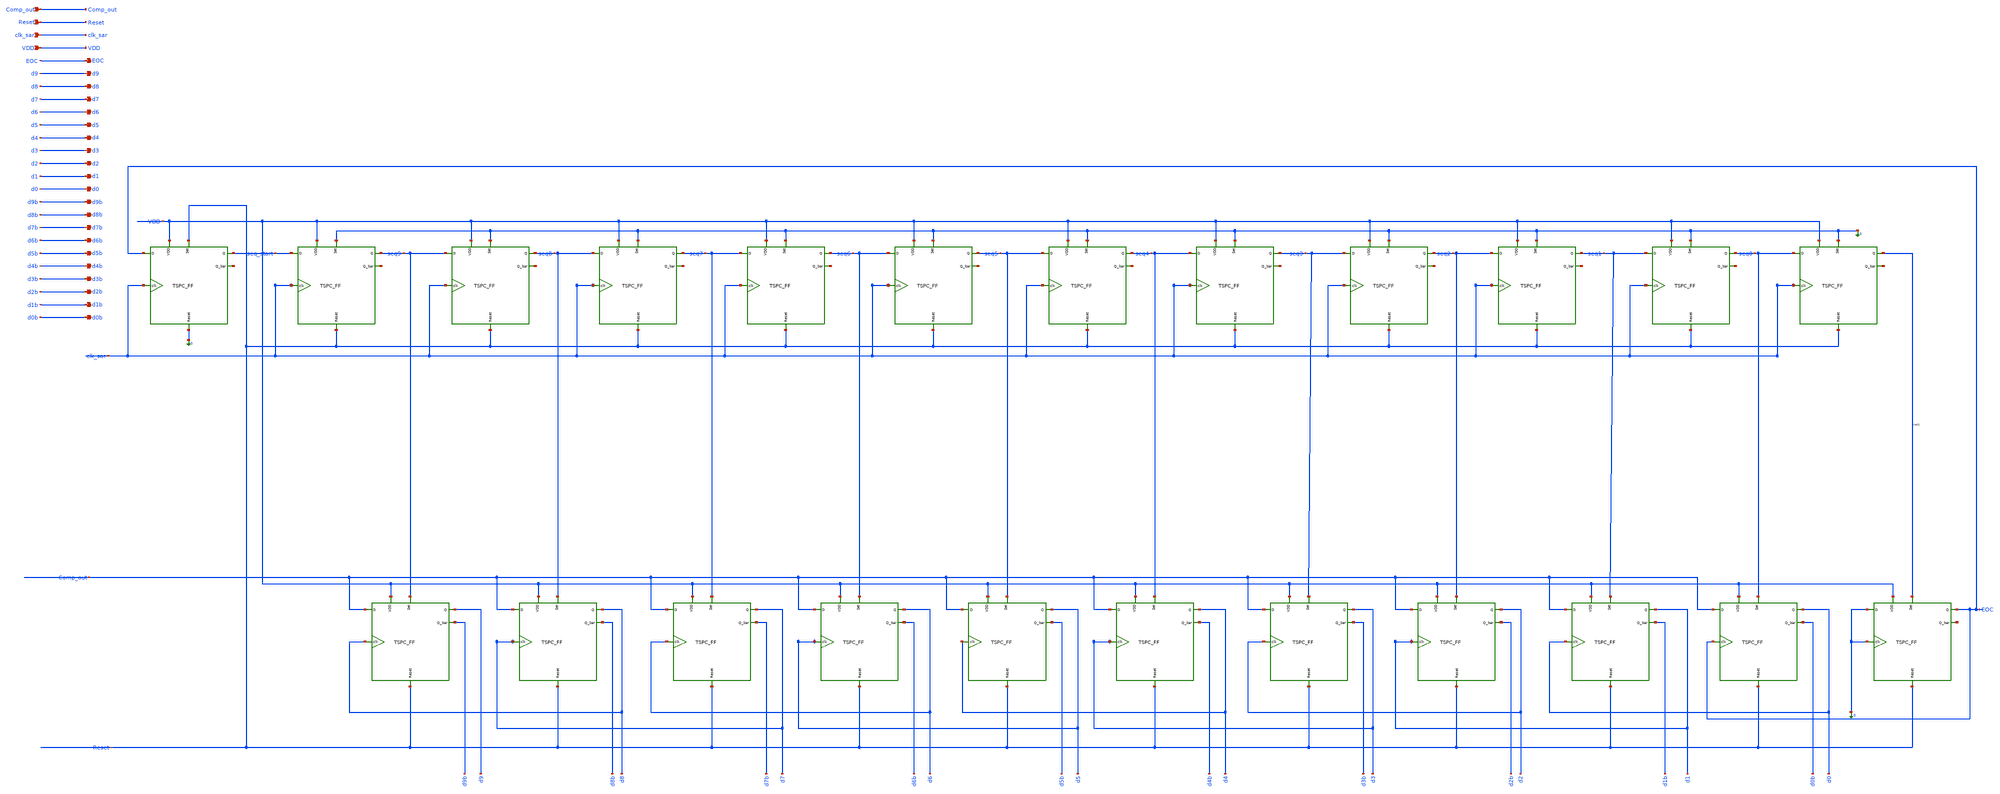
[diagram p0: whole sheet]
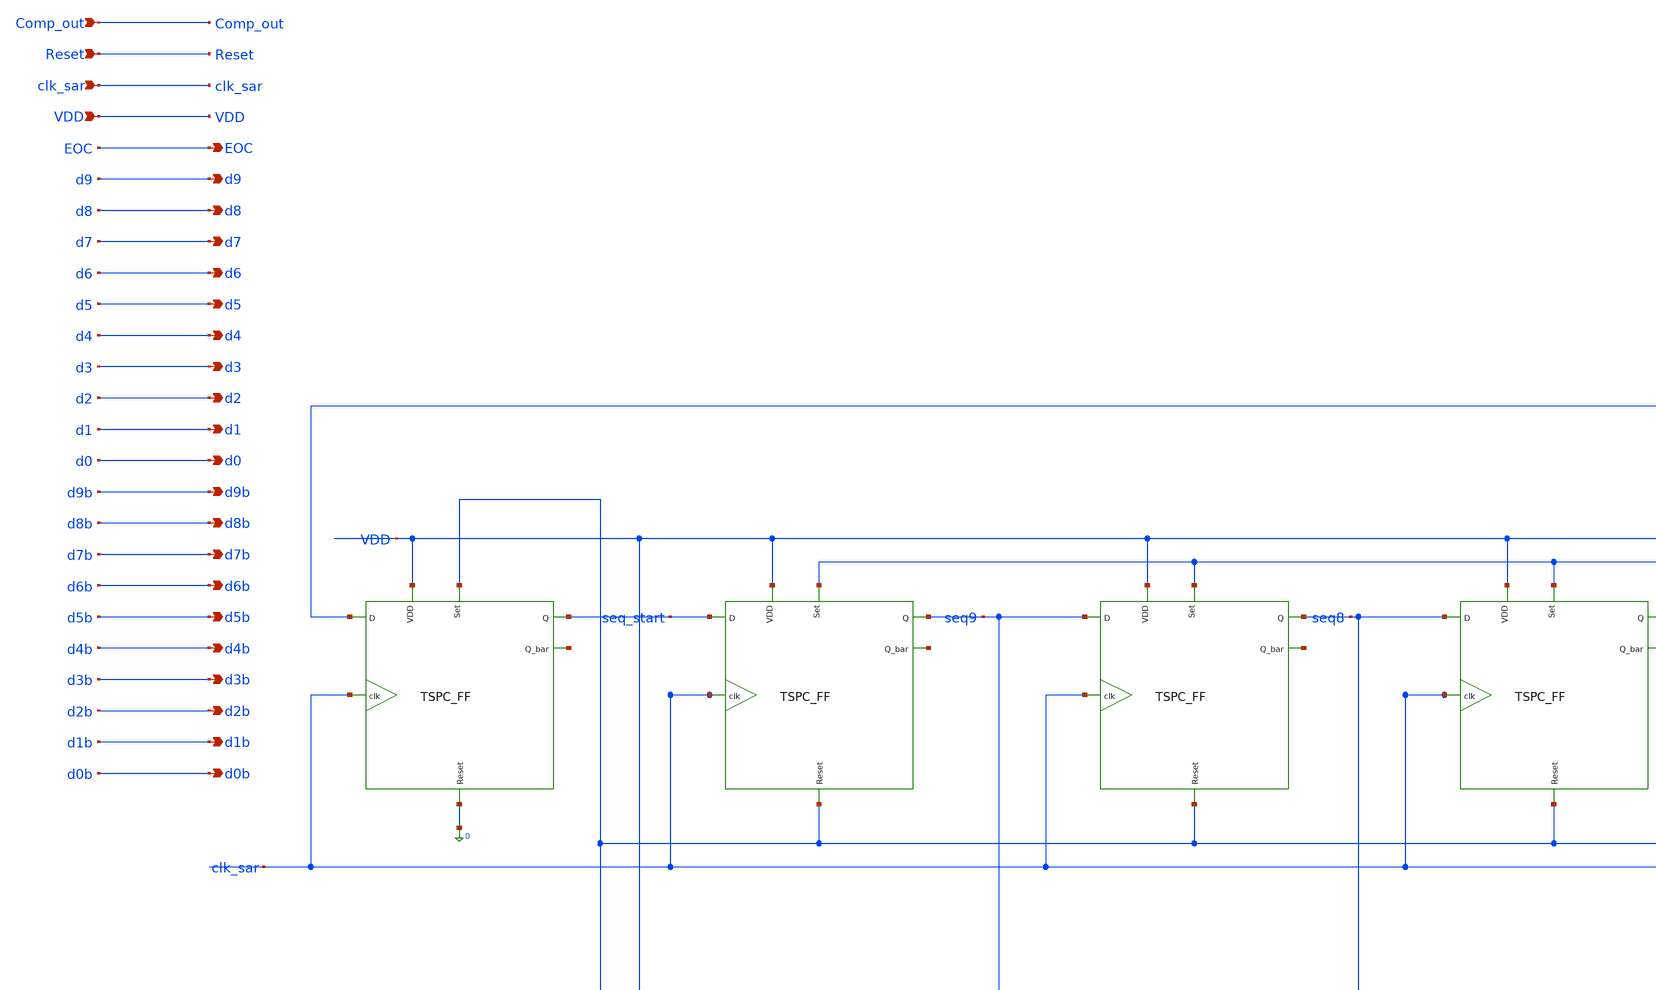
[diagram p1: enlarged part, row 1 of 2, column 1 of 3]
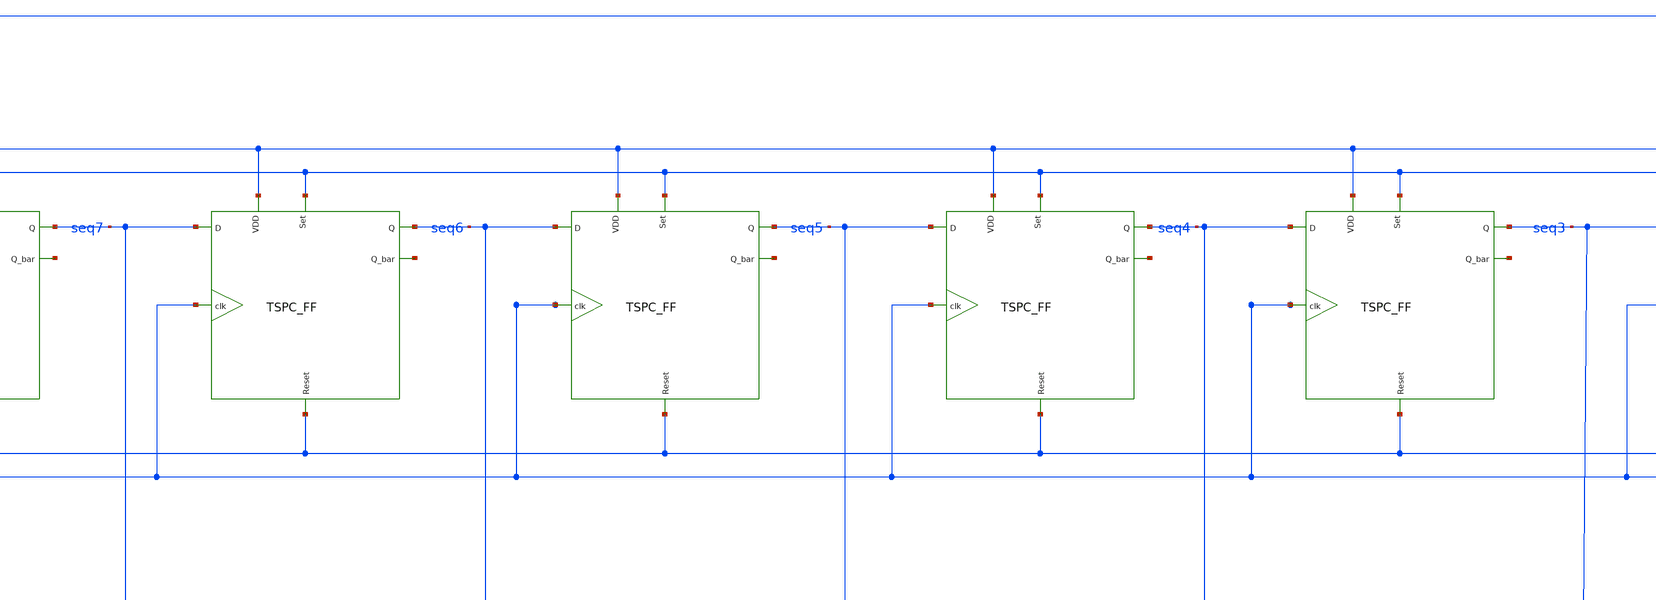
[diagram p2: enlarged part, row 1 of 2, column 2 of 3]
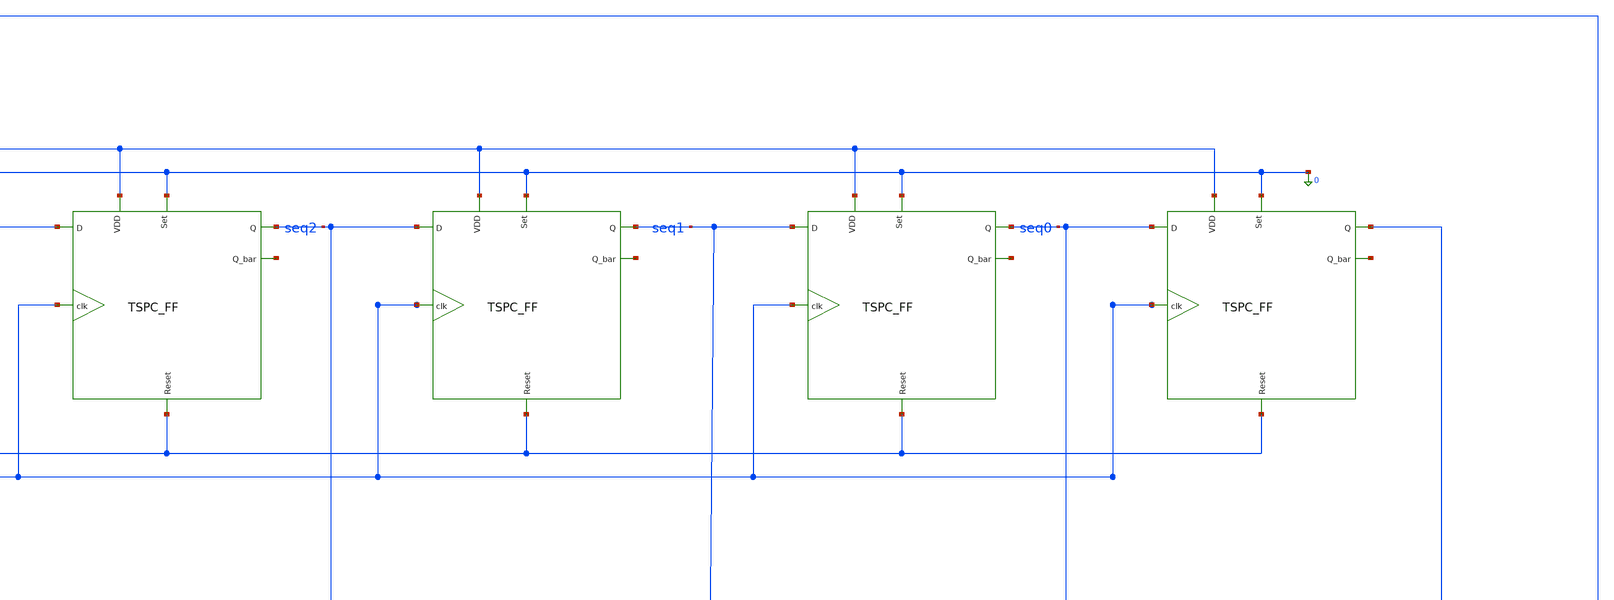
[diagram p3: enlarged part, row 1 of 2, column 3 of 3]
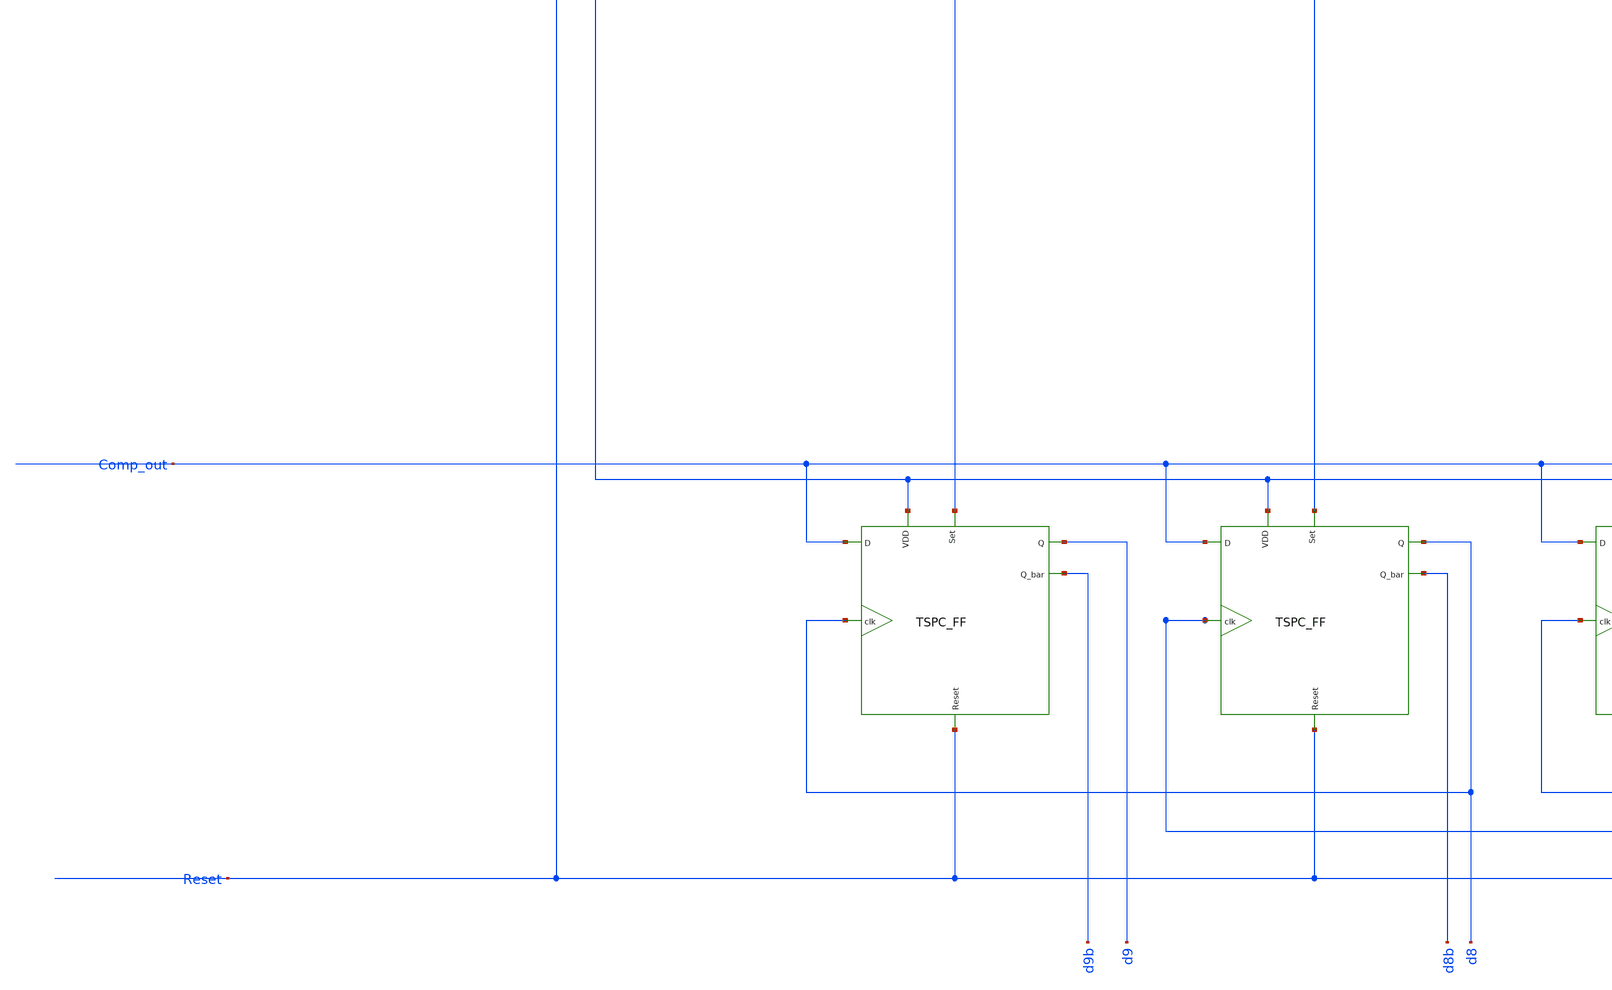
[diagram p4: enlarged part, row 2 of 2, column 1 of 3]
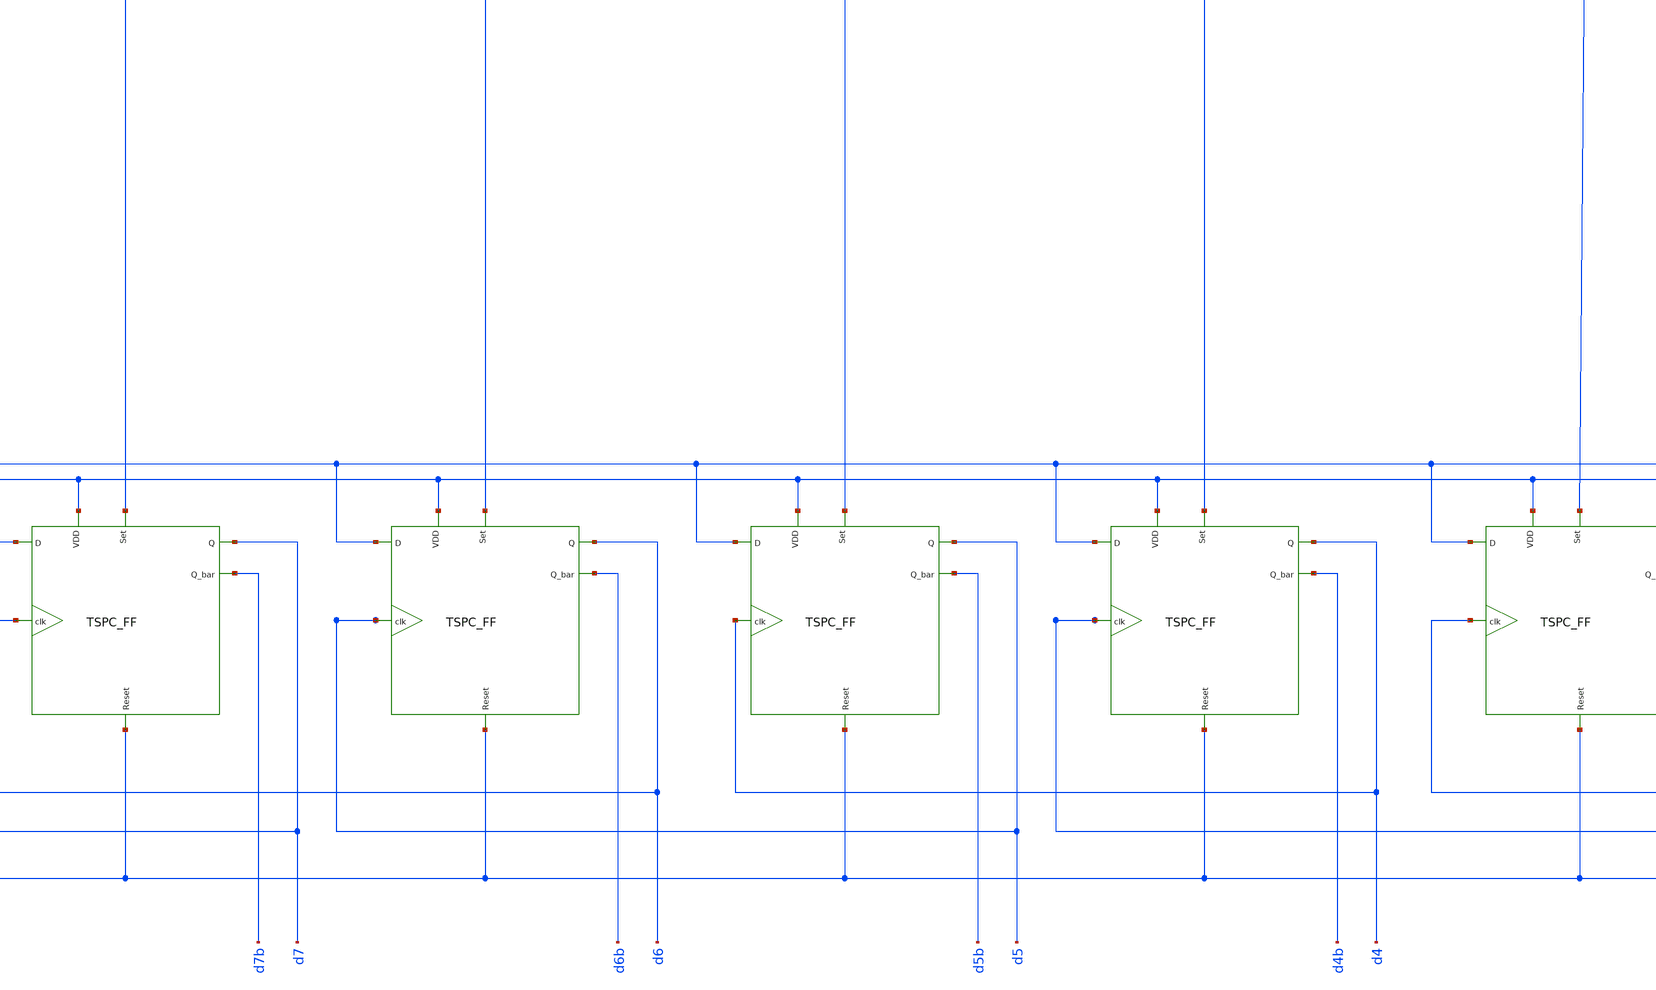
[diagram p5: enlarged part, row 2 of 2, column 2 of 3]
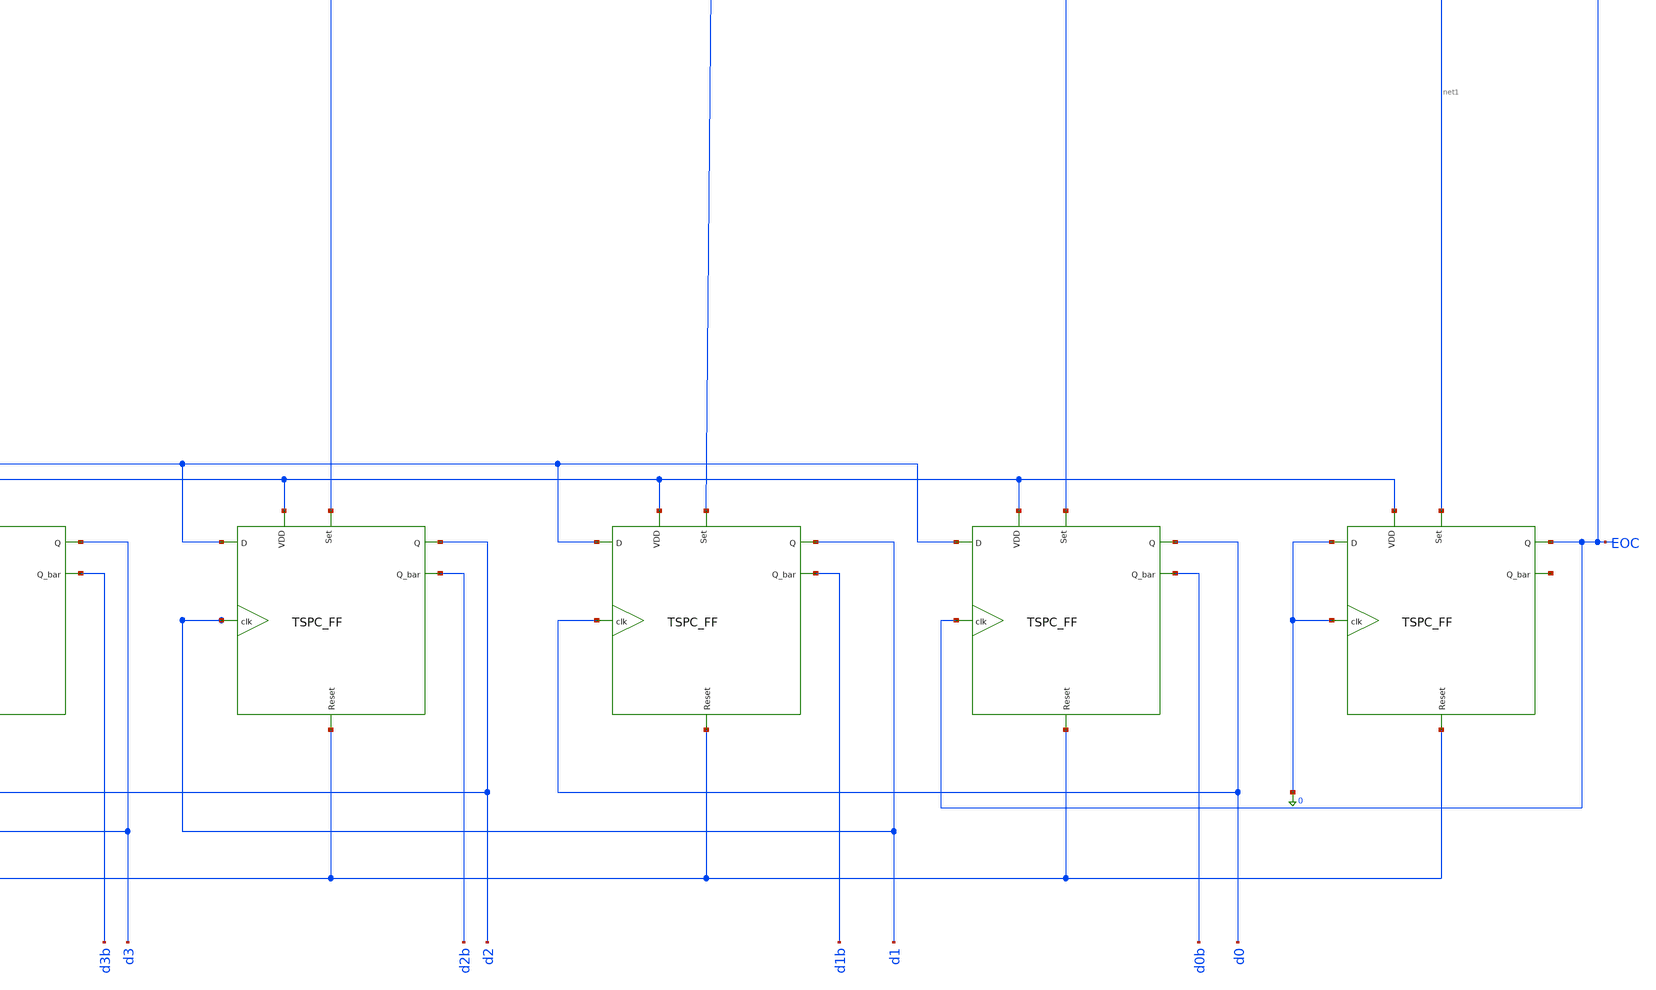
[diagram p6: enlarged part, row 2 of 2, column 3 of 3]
** sch_path: Design_Files/IC Design/Schematic/SAR_ADC_BLOCKS/SAR_LOGIC/SAR_LOGIC.sch
**.subckt SAR_LOGIC Comp_out Reset clk_sar VDD EOC d7 d6 d5 d4 d3 d2 d1 d0 d9 d8 d7b d6b d5b d4b d3b
*+ d2b d1b d0b d9b d8b
*.ipin Comp_out
*.ipin Reset
*.ipin clk_sar
*.ipin VDD
*.opin EOC
*.opin d7
*.opin d6
*.opin d5
*.opin d4
*.opin d3
*.opin d2
*.opin d1
*.opin d0
*.opin d9
*.opin d8
*.opin d7b
*.opin d6b
*.opin d5b
*.opin d4b
*.opin d3b
*.opin d2b
*.opin d1b
*.opin d0b
*.opin d9b
*.opin d8b
xTSPCFF1 EOC clk_sar VDD Reset 0 seq_start net2 TSPC_FF
xTSPCFF2 seq_start clk_sar VDD 0 Reset seq9 net3 TSPC_FF
xTSPCFF3 seq9 clk_sar VDD 0 Reset seq8 net4 TSPC_FF
xTSPCFF4 seq8 clk_sar VDD 0 Reset seq7 net5 TSPC_FF
xTSPCFF5 seq7 clk_sar VDD 0 Reset seq6 net6 TSPC_FF
xTSPCFF6 seq6 clk_sar VDD 0 Reset seq5 net7 TSPC_FF
xTSPCFF7 seq5 clk_sar VDD 0 Reset seq4 net8 TSPC_FF
xTSPCFF8 seq4 clk_sar VDD 0 Reset seq3 net9 TSPC_FF
xTSPCFF9 seq3 clk_sar VDD 0 Reset seq2 net10 TSPC_FF
xTSPCFF10 seq2 clk_sar VDD 0 Reset seq1 net11 TSPC_FF
xTSPCFF11 seq1 clk_sar VDD 0 Reset seq0 net12 TSPC_FF
xTSPCFF12 seq0 clk_sar VDD 0 Reset net1 net13 TSPC_FF
xTSPCFF13 Comp_out d8 VDD seq9 Reset d9 d9b TSPC_FF
xTSPCFF14 Comp_out d7 VDD seq8 Reset d8 d8b TSPC_FF
xTSPCFF15 Comp_out d6 VDD seq7 Reset d7 d7b TSPC_FF
xTSPCFF16 Comp_out d5 VDD seq6 Reset d6 d6b TSPC_FF
xTSPCFF17 Comp_out d4 VDD seq5 Reset d5 d5b TSPC_FF
xTSPCFF18 Comp_out d3 VDD seq4 Reset d4 d4b TSPC_FF
xTSPCFF19 Comp_out d2 VDD seq3 Reset d3 d3b TSPC_FF
xTSPCFF20 Comp_out d1 VDD seq2 Reset d2 d2b TSPC_FF
xTSPCFF21 Comp_out d0 VDD seq1 Reset d1 d1b TSPC_FF
xTSPCFF22 Comp_out EOC VDD seq0 Reset d0 d0b TSPC_FF
xTSPCFF23 0 0 VDD net1 Reset EOC net14 TSPC_FF
**.ends

* expanding   symbol:  ECG_Acquisition_IC/Design_Files/IC
*+ Design/Schematic/SAR_ADC_BLOCKS/TSPC_FF/TSPC_FF.sym # of pins=7
** sym_path: Design_Files/IC Design/Schematic/SAR_ADC_BLOCKS/TSPC_FF/TSPC_FF.sym
** sch_path: Design_Files/IC Design/Schematic/SAR_ADC_BLOCKS/TSPC_FF/TSPC_FF.sch
.subckt TSPC_FF D clk VDD Set Reset Q Q_bar
*.ipin D
*.ipin clk
*.ipin VDD
*.ipin Set
*.ipin Reset
*.opin Q
*.opin Q_bar
XM1 net1 D VDD VDD pfet_03v3 L=0.28u W=5.10u nf=1 ad='int((nf+1)/2) * W/nf * 0.18u' as='int((nf+2)/2) * W/nf * 0.18u'
+ pd='2*int((nf+1)/2) * (W/nf + 0.18u)' ps='2*int((nf+2)/2) * (W/nf + 0.18u)' nrd='0.18u / W' nrs='0.18u / W'
+ sa=0 sb=0 sd=0 m=1
XM2 Q_1st clk net1 VDD pfet_03v3 L=0.28u W=6.12u nf=1 ad='int((nf+1)/2) * W/nf * 0.18u' as='int((nf+2)/2) * W/nf * 0.18u'
+ pd='2*int((nf+1)/2) * (W/nf + 0.18u)' ps='2*int((nf+2)/2) * (W/nf + 0.18u)' nrd='0.18u / W' nrs='0.18u / W'
+ sa=0 sb=0 sd=0 m=1
XM3 Q_1st D 0 0 nfet_03v3 L=0.28u W=1u nf=1 ad='int((nf+1)/2) * W/nf * 0.18u' as='int((nf+2)/2) * W/nf * 0.18u'
+ pd='2*int((nf+1)/2) * (W/nf + 0.18u)' ps='2*int((nf+2)/2) * (W/nf + 0.18u)' nrd='0.18u / W' nrs='0.18u / W'
+ sa=0 sb=0 sd=0 m=1
XM4 Q_pre clk VDD VDD pfet_03v3 L=0.28u W=10u nf=1 ad='int((nf+1)/2) * W/nf * 0.18u' as='int((nf+2)/2) * W/nf * 0.18u'
+ pd='2*int((nf+1)/2) * (W/nf + 0.18u)' ps='2*int((nf+2)/2) * (W/nf + 0.18u)' nrd='0.18u / W' nrs='0.18u / W'
+ sa=0 sb=0 sd=0 m=1
XM6 net2 clk 0 0 nfet_03v3 L=0.28u W=4u nf=1 ad='int((nf+1)/2) * W/nf * 0.18u' as='int((nf+2)/2) * W/nf * 0.18u'
+ pd='2*int((nf+1)/2) * (W/nf + 0.18u)' ps='2*int((nf+2)/2) * (W/nf + 0.18u)' nrd='0.18u / W' nrs='0.18u / W'
+ sa=0 sb=0 sd=0 m=1
XM7 net3 Q_pre VDD VDD pfet_03v3 L=0.28u W=5.10u nf=1 ad='int((nf+1)/2) * W/nf * 0.18u' as='int((nf+2)/2) * W/nf * 0.18u'
+ pd='2*int((nf+1)/2) * (W/nf + 0.18u)' ps='2*int((nf+2)/2) * (W/nf + 0.18u)' nrd='0.18u / W' nrs='0.18u / W'
+ sa=0 sb=0 sd=0 m=1
XM8 Q_bar_pre Set net3 VDD pfet_03v3 L=0.28u W=6.12u nf=1 ad='int((nf+1)/2) * W/nf * 0.18u' as='int((nf+2)/2) * W/nf * 0.18u'
+ pd='2*int((nf+1)/2) * (W/nf + 0.18u)' ps='2*int((nf+2)/2) * (W/nf + 0.18u)' nrd='0.18u / W' nrs='0.18u / W'
+ sa=0 sb=0 sd=0 m=1
XM9 Q_bar_pre clk net4 0 nfet_03v3 L=0.28u W=1.72u nf=1 ad='int((nf+1)/2) * W/nf * 0.18u' as='int((nf+2)/2) * W/nf * 0.18u'
+ pd='2*int((nf+1)/2) * (W/nf + 0.18u)' ps='2*int((nf+2)/2) * (W/nf + 0.18u)' nrd='0.18u / W' nrs='0.18u / W'
+ sa=0 sb=0 sd=0 m=1
XM10 net4 Q_pre net6 0 nfet_03v3 L=0.28u W=1.5u nf=1 ad='int((nf+1)/2) * W/nf * 0.18u' as='int((nf+2)/2) * W/nf * 0.18u'
+ pd='2*int((nf+1)/2) * (W/nf + 0.18u)' ps='2*int((nf+2)/2) * (W/nf + 0.18u)' nrd='0.18u / W' nrs='0.18u / W'
+ sa=0 sb=0 sd=0 m=1
XM11 Q_bar_pre net5 VDD VDD pfet_03v3 L=0.28u W=2u nf=1 ad='int((nf+1)/2) * W/nf * 0.18u' as='int((nf+2)/2) * W/nf * 0.18u'
+ pd='2*int((nf+1)/2) * (W/nf + 0.18u)' ps='2*int((nf+2)/2) * (W/nf + 0.18u)' nrd='0.18u / W' nrs='0.18u / W'
+ sa=0 sb=0 sd=0 m=1
XM12 Q_bar_pre Set 0 0 nfet_03v3 L=0.28u W=0.25u nf=1 ad='int((nf+1)/2) * W/nf * 0.18u' as='int((nf+2)/2) * W/nf * 0.18u'
+ pd='2*int((nf+1)/2) * (W/nf + 0.18u)' ps='2*int((nf+2)/2) * (W/nf + 0.18u)' nrd='0.18u / W' nrs='0.18u / W'
+ sa=0 sb=0 sd=0 m=1
XM13 Q Q_bar_pre VDD VDD pfet_03v3 L=0.28u W=0.425u nf=1 ad='int((nf+1)/2) * W/nf * 0.18u' as='int((nf+2)/2) * W/nf * 0.18u'
+ pd='2*int((nf+1)/2) * (W/nf + 0.18u)' ps='2*int((nf+2)/2) * (W/nf + 0.18u)' nrd='0.18u / W' nrs='0.18u / W'
+ sa=0 sb=0 sd=0 m=1
XM14 Q Q_bar_pre 0 0 nfet_03v3 L=0.56u W=0.5u nf=1 ad='int((nf+1)/2) * W/nf * 0.18u' as='int((nf+2)/2) * W/nf * 0.18u'
+ pd='2*int((nf+1)/2) * (W/nf + 0.18u)' ps='2*int((nf+2)/2) * (W/nf + 0.18u)' nrd='0.18u / W' nrs='0.18u / W'
+ sa=0 sb=0 sd=0 m=1
XM15 Q_bar Q VDD VDD pfet_03v3 L=0.28u W=0.22u nf=1 ad='int((nf+1)/2) * W/nf * 0.18u' as='int((nf+2)/2) * W/nf * 0.18u'
+ pd='2*int((nf+1)/2) * (W/nf + 0.18u)' ps='2*int((nf+2)/2) * (W/nf + 0.18u)' nrd='0.18u / W' nrs='0.18u / W'
+ sa=0 sb=0 sd=0 m=1
XM16 Q_bar Q 0 0 nfet_03v3 L=0.28u W=0.22u nf=1 ad='int((nf+1)/2) * W/nf * 0.18u' as='int((nf+2)/2) * W/nf * 0.18u'
+ pd='2*int((nf+1)/2) * (W/nf + 0.18u)' ps='2*int((nf+2)/2) * (W/nf + 0.18u)' nrd='0.18u / W' nrs='0.18u / W'
+ sa=0 sb=0 sd=0 m=1
XM17 net6 net7 0 0 nfet_03v3 L=0.28u W=1.5u nf=1 ad='int((nf+1)/2) * W/nf * 0.18u' as='int((nf+2)/2) * W/nf * 0.18u'
+ pd='2*int((nf+1)/2) * (W/nf + 0.18u)' ps='2*int((nf+2)/2) * (W/nf + 0.18u)' nrd='0.18u / W' nrs='0.18u / W'
+ sa=0 sb=0 sd=0 m=1
xINV1_1 Reset VDD net7 INV
xINV1_2 Reset VDD net5 INV
XM5 Q_pre Q_1st net2 0 nfet_03v3 L=0.28u W=4u nf=1 ad='int((nf+1)/2) * W/nf * 0.18u' as='int((nf+2)/2) * W/nf * 0.18u'
+ pd='2*int((nf+1)/2) * (W/nf + 0.18u)' ps='2*int((nf+2)/2) * (W/nf + 0.18u)' nrd='0.18u / W' nrs='0.18u / W'
+ sa=0 sb=0 sd=0 m=1
.ends


* expanding   symbol:  ECG_Acquisition_IC/Design_Files/IC
*+ Design/Schematic/SAR_ADC_BLOCKS/INV/INV.sym # of pins=3
** sym_path: Design_Files/IC Design/Schematic/SAR_ADC_BLOCKS/INV/INV.sym
** sch_path: Design_Files/IC Design/Schematic/SAR_ADC_BLOCKS/INV/INV.sch
.subckt INV in VDD out
*.ipin in
*.ipin VDD
*.opin out
XM1 out in 0 0 nfet_03v3 L=0.28u W=0.22u nf=1 ad='int((nf+1)/2) * W/nf * 0.18u' as='int((nf+2)/2) * W/nf * 0.18u'
+ pd='2*int((nf+1)/2) * (W/nf + 0.18u)' ps='2*int((nf+2)/2) * (W/nf + 0.18u)' nrd='0.18u / W' nrs='0.18u / W'
+ sa=0 sb=0 sd=0 m=wn_inv
XM2 out in vdd vdd pfet_03v3 L=0.28u W=0.22u nf=1 ad='int((nf+1)/2) * W/nf * 0.18u' as='int((nf+2)/2) * W/nf * 0.18u'
+ pd='2*int((nf+1)/2) * (W/nf + 0.18u)' ps='2*int((nf+2)/2) * (W/nf + 0.18u)' nrd='0.18u / W' nrs='0.18u / W'
+ sa=0 sb=0 sd=0 m=wp_inv
.ends

.end
